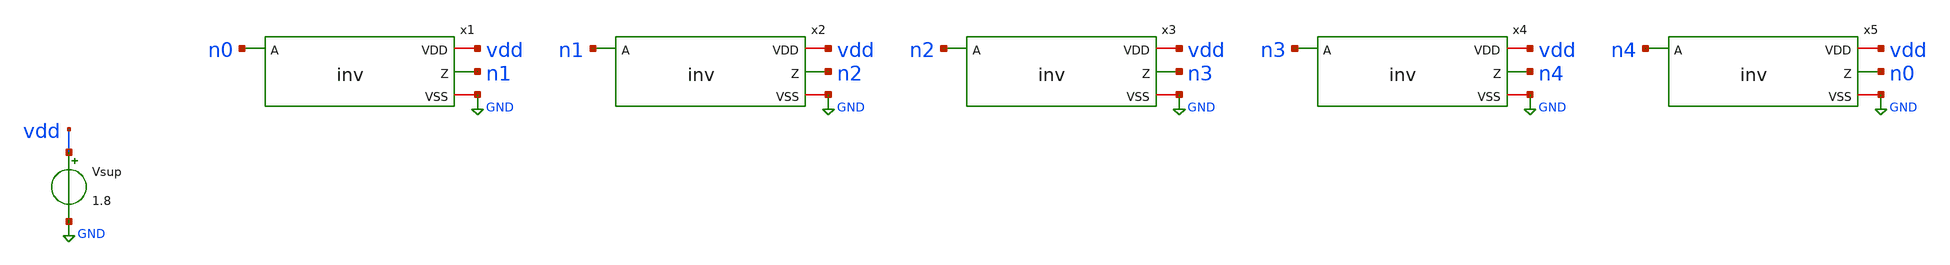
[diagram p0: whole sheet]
** sch_path: pipeline/analog/ring/ringosc_tb.sch
**.subckt ringosc_tb
x1 n0 vdd n1 GND inv
x2 n1 vdd n2 GND inv
x3 n2 vdd n3 GND inv
x4 n3 vdd n4 GND inv
x5 n4 vdd n0 GND inv
Vsup vdd GND 1.8
**** begin user architecture code


%PDK_LIB%



.param W_P=1.4266 W_N=0.5 L_P=0.15 L_N=0.15
.ic v(n0)=0
.control
tran 5p 20n
meas tran period TRIG v(n0) VAL=0.9 RISE=2 TARG v(n0) VAL=0.9 RISE=3
meas tran isup_avg AVG i(Vsup) FROM=5n TO=20n
quit
.endc


**** end user architecture code
**.ends

* expanding   symbol:  inv/inv.sym # of pins=4
** sym_path: pipeline/analog/inv/inv.sym
** sch_path: pipeline/analog/inv/inv.sch
.subckt inv A VDD Z VSS
*.ipin A
*.opin Z
*.iopin VDD
*.iopin VSS
XM1 Z A VSS VSS sky130_fd_pr__nfet_01v8 L=L_N W=W_N nf=1 ad='int((nf+1)/2) * W/nf * 0.29' as='int((nf+2)/2) * W/nf * 0.29'
+ pd='2*int((nf+1)/2) * (W/nf + 0.29)' ps='2*int((nf+2)/2) * (W/nf + 0.29)' nrd='0.29 / W' nrs='0.29 / W'
+ sa=0 sb=0 sd=0 mult=1 m=1
XM2 Z A VDD VDD sky130_fd_pr__pfet_01v8 L=L_P W=W_P nf=1 ad='int((nf+1)/2) * W/nf * 0.29' as='int((nf+2)/2) * W/nf * 0.29'
+ pd='2*int((nf+1)/2) * (W/nf + 0.29)' ps='2*int((nf+2)/2) * (W/nf + 0.29)' nrd='0.29 / W' nrs='0.29 / W'
+ sa=0 sb=0 sd=0 mult=1 m=1
.ends

.GLOBAL GND
.end
